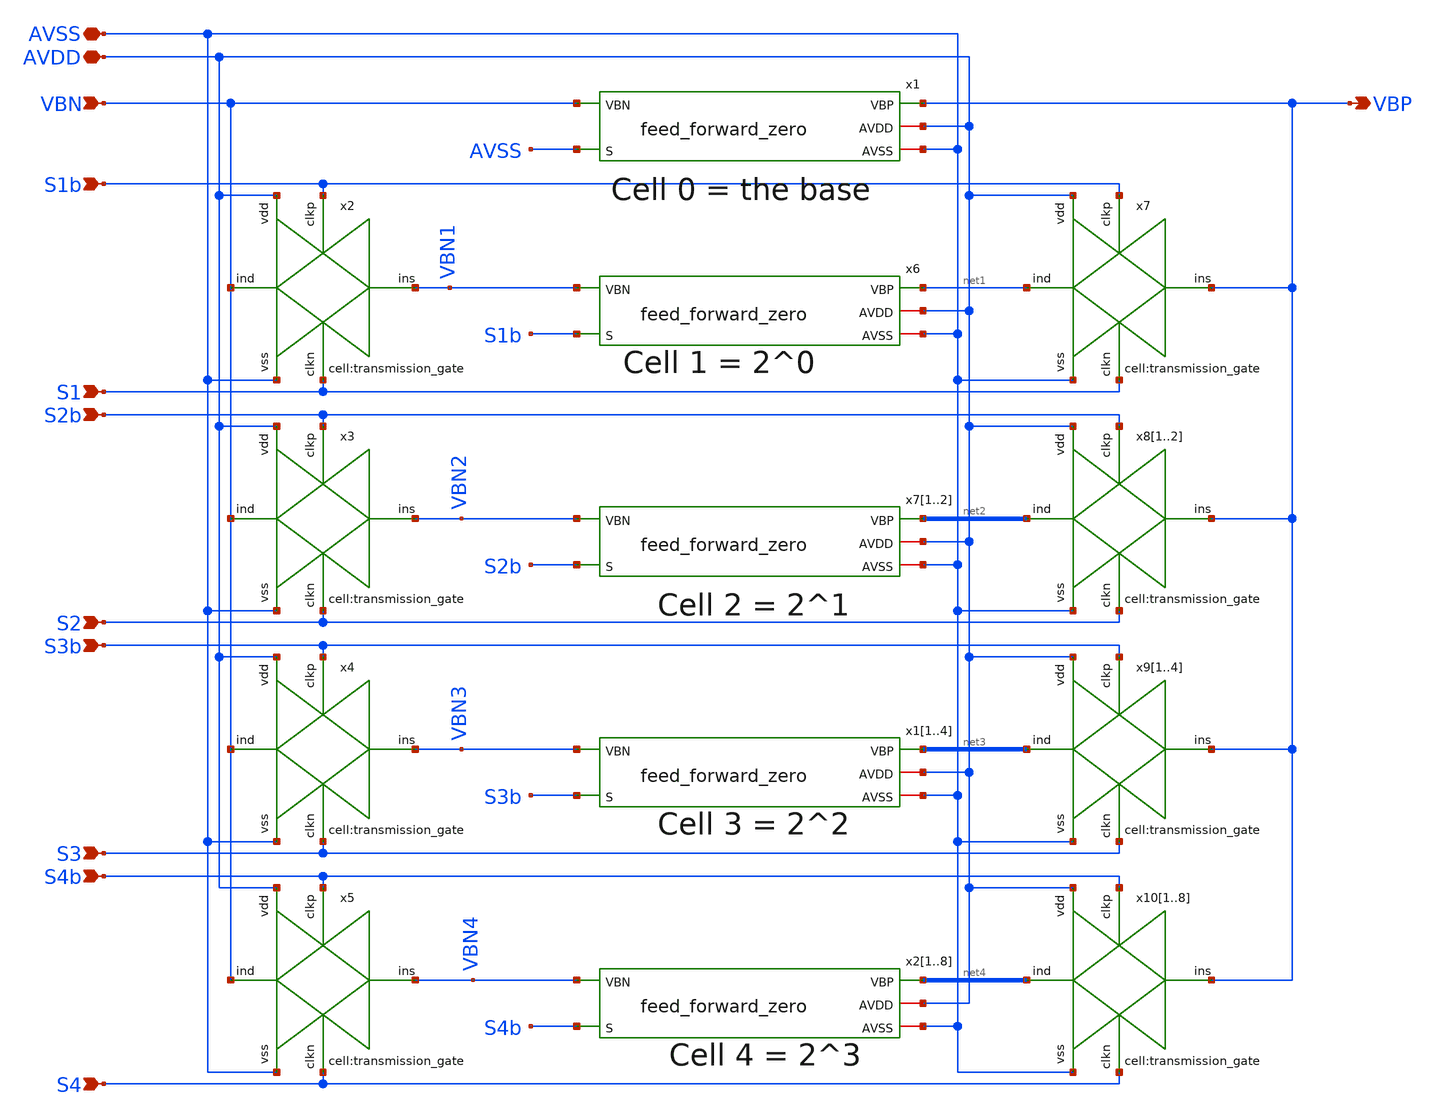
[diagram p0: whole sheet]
** sch_path: designs/libs/core_analog/programmable_ffz/programmable_ffz.sch
**.subckt programmable_ffz VBN S1b S1 S2b S2 S3b S3 S4b S4 AVSS AVDD VBP
*.ipin VBN
*.ipin S1b
*.ipin S1
*.ipin S2b
*.ipin S2
*.ipin S3b
*.ipin S3
*.ipin S4b
*.ipin S4
*.iopin AVSS
*.iopin AVDD
*.opin VBP
x2 VBN AVSS S1 VBN1 S1b AVDD transmission_gate
x3 VBN AVSS S2 VBN2 S2b AVDD transmission_gate
x4 VBN AVSS S3 VBN3 S3b AVDD transmission_gate
x5 VBN AVSS S4 VBN4 S4b AVDD transmission_gate
x1 AVDD VBP VBN AVSS AVSS feed_forward_zero
x6 AVDD net1 VBN1 S1b AVSS feed_forward_zero
x71 AVDD net2[1] VBN2 S2b AVSS feed_forward_zero
x72 AVDD net2[0] VBN2 S2b AVSS feed_forward_zero
x11 AVDD net3[3] VBN3 S3b AVSS feed_forward_zero
x12 AVDD net3[2] VBN3 S3b AVSS feed_forward_zero
x13 AVDD net3[1] VBN3 S3b AVSS feed_forward_zero
x14 AVDD net3[0] VBN3 S3b AVSS feed_forward_zero
x21 AVDD net4[7] VBN4 S4b AVSS feed_forward_zero
x22 AVDD net4[6] VBN4 S4b AVSS feed_forward_zero
x23 AVDD net4[5] VBN4 S4b AVSS feed_forward_zero
x24 AVDD net4[4] VBN4 S4b AVSS feed_forward_zero
x25 AVDD net4[3] VBN4 S4b AVSS feed_forward_zero
x26 AVDD net4[2] VBN4 S4b AVSS feed_forward_zero
x27 AVDD net4[1] VBN4 S4b AVSS feed_forward_zero
x28 AVDD net4[0] VBN4 S4b AVSS feed_forward_zero
x7 net1 AVSS S1 VBP S1b AVDD transmission_gate
x81 net2[1] AVSS S2 VBP S2b AVDD transmission_gate
x82 net2[0] AVSS S2 VBP S2b AVDD transmission_gate
x91 net3[3] AVSS S3 VBP S3b AVDD transmission_gate
x92 net3[2] AVSS S3 VBP S3b AVDD transmission_gate
x93 net3[1] AVSS S3 VBP S3b AVDD transmission_gate
x94 net3[0] AVSS S3 VBP S3b AVDD transmission_gate
x101 net4[7] AVSS S4 VBP S4b AVDD transmission_gate
x102 net4[6] AVSS S4 VBP S4b AVDD transmission_gate
x103 net4[5] AVSS S4 VBP S4b AVDD transmission_gate
x104 net4[4] AVSS S4 VBP S4b AVDD transmission_gate
x105 net4[3] AVSS S4 VBP S4b AVDD transmission_gate
x106 net4[2] AVSS S4 VBP S4b AVDD transmission_gate
x107 net4[1] AVSS S4 VBP S4b AVDD transmission_gate
x108 net4[0] AVSS S4 VBP S4b AVDD transmission_gate
**.ends

* expanding   symbol:  libs/core_analog/transmission_gate/transmission_gate.sym # of pins=6
** sym_path: designs/libs/core_analog/transmission_gate/transmission_gate.sym
** sch_path: designs/libs/core_analog/transmission_gate/transmission_gate.sch
.subckt transmission_gate ind vss clkn ins clkp vdd
*.iopin ind
*.iopin ins
*.iopin clkn
*.iopin clkp
*.iopin vdd
*.iopin vss
XM1 ind clkp ins vdd pfet_03v3 L=0.5u W=3.0u nf=1 ad='int((nf+1)/2) * W/nf * 0.18u' as='int((nf+2)/2) * W/nf * 0.18u'
+ pd='2*int((nf+1)/2) * (W/nf + 0.18u)' ps='2*int((nf+2)/2) * (W/nf + 0.18u)' nrd='0.18u / W' nrs='0.18u / W'
+ sa=0 sb=0 sd=0 m=1
XM2 ind clkn ins vss nfet_03v3 L=0.5u W=1.0u nf=1 ad='int((nf+1)/2) * W/nf * 0.18u' as='int((nf+2)/2) * W/nf * 0.18u'
+ pd='2*int((nf+1)/2) * (W/nf + 0.18u)' ps='2*int((nf+2)/2) * (W/nf + 0.18u)' nrd='0.18u / W' nrs='0.18u / W'
+ sa=0 sb=0 sd=0 m=1
.ends


* expanding   symbol:  libs/core_analog/feed_forward_zero/feed_forward_zero.sym # of pins=5
** sym_path: designs/libs/core_analog/feed_forward_zero/feed_forward_zero.sym
** sch_path: designs/libs/core_analog/feed_forward_zero/feed_forward_zero.sch
.subckt feed_forward_zero AVDD VBP VBN S AVSS
*.opin VBP
*.iopin AVDD
*.iopin AVSS
*.ipin VBN
*.ipin S
XM1 VBP VBP AVDD AVDD pfet_03v3 L=1.5u W=1.1u nf=1 ad='int((nf+1)/2) * W/nf * 0.18u' as='int((nf+2)/2) * W/nf * 0.18u'
+ pd='2*int((nf+1)/2) * (W/nf + 0.18u)' ps='2*int((nf+2)/2) * (W/nf + 0.18u)' nrd='0.18u / W' nrs='0.18u / W'
+ sa=0 sb=0 sd=0 m=2
XM2 VBP VBP AVDD AVDD pfet_03v3 L=1.5u W=1.1u nf=1 ad='int((nf+1)/2) * W/nf * 0.18u' as='int((nf+2)/2) * W/nf * 0.18u'
+ pd='2*int((nf+1)/2) * (W/nf + 0.18u)' ps='2*int((nf+2)/2) * (W/nf + 0.18u)' nrd='0.18u / W' nrs='0.18u / W'
+ sa=0 sb=0 sd=0 m=2
XM3 VBP AVDD net1 AVSS nfet_03v3 L=0.5u W=2.08u nf=1 ad='int((nf+1)/2) * W/nf * 0.18u' as='int((nf+2)/2) * W/nf * 0.18u'
+ pd='2*int((nf+1)/2) * (W/nf + 0.18u)' ps='2*int((nf+2)/2) * (W/nf + 0.18u)' nrd='0.18u / W' nrs='0.18u / W'
+ sa=0 sb=0 sd=0 m=2
XM4 net1 VBN AVSS AVSS nfet_03v3 L=0.5u W=11.25u nf=1 ad='int((nf+1)/2) * W/nf * 0.18u' as='int((nf+2)/2) * W/nf * 0.18u'
+ pd='2*int((nf+1)/2) * (W/nf + 0.18u)' ps='2*int((nf+2)/2) * (W/nf + 0.18u)' nrd='0.18u / W' nrs='0.18u / W'
+ sa=0 sb=0 sd=0 m=2
XM7 VBN S AVSS AVSS nfet_03v3 L=0.5u W=1u nf=1 ad='int((nf+1)/2) * W/nf * 0.18u' as='int((nf+2)/2) * W/nf * 0.18u'
+ pd='2*int((nf+1)/2) * (W/nf + 0.18u)' ps='2*int((nf+2)/2) * (W/nf + 0.18u)' nrd='0.18u / W' nrs='0.18u / W'
+ sa=0 sb=0 sd=0 m=1
.ends

.end
